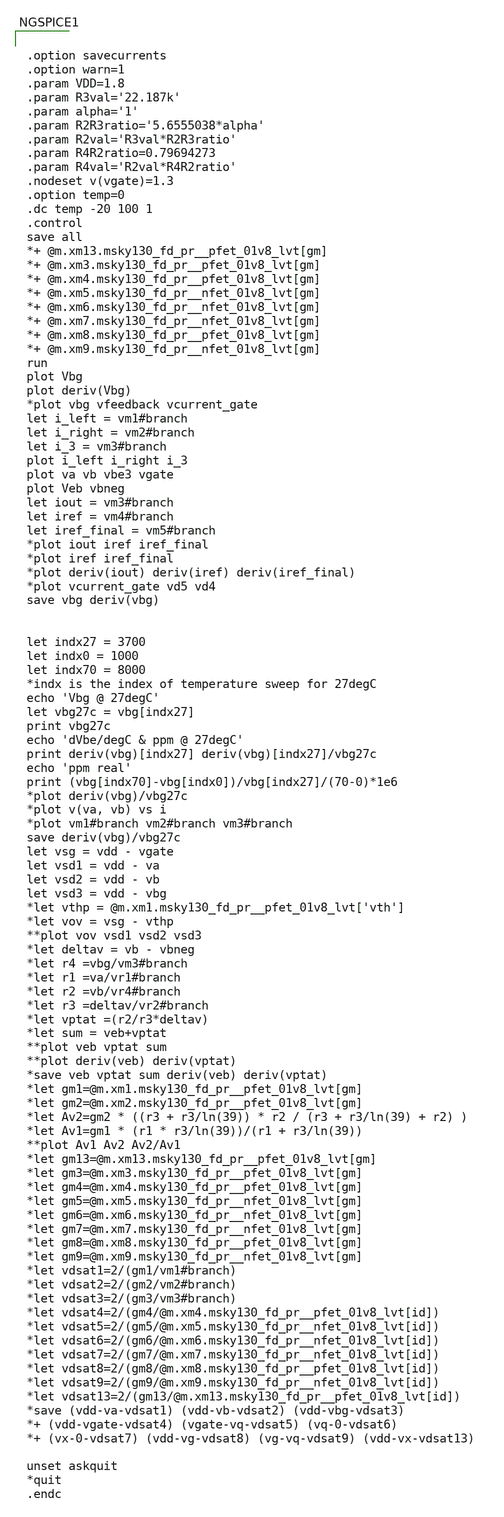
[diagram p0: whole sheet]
** sch_path: scratch.sch
**.subckt scratch
**** begin user architecture code


.options savecurrents


.option
.control
save all
let startR = 20k
let endR = 30k
let incre = 1k
let curR = startR
while curR le endR
alter Rt curR
dc temp -40 100 1
write dc.out Vbg
set appendwrite
let curR = curR + incre
end
run

plot dc1.Vbg dc2.Vbg dc3.Vbg dc4.Vbg dc5.Vbg dc6.Vbg dc7.Vbg dc8.Vbg dc9.Vbg dc10.Vbg


.endc

*** plot voltage coefficient
*Vdd VDD GND 3.3
*V_en en GND 3.3
*.dc Vdd 2 4 0.1
*.control
*run
*plot deriv(V(Vbgp))
*.endc

*** plot temperature coefficient
*Vdd VDD GND 3.3
*V_en en GND 3.3
*.dc temp -40 140 1
*.control
*run
*plot deriv(V(Vbgp))/1.202344
*.endc



*** enable pin
*Vdd VDD GND 3.3
*V_en en GND PULSE(0 3.3 0 200us 200us 600us 2000us 0)
*.tran 1u 2000us
*.control
*run
*plot V(en)
*plot -I(VDD)
*.endc




.option savecurrents
.option warn=1
.param VDD=1.8
.param R3val='22.187k'
.param alpha='1'
.param R2R3ratio='5.6555038*alpha'
.param R2val='R3val*R2R3ratio'
.param R4R2ratio=0.79694273
.param R4val='R2val*R4R2ratio'
.nodeset v(vgate)=1.3
.option temp=0
.dc temp -20 100 1
.control
save all
*+ @m.xm13.msky130_fd_pr__pfet_01v8_lvt[gm]
*+ @m.xm3.msky130_fd_pr__pfet_01v8_lvt[gm]
*+ @m.xm4.msky130_fd_pr__pfet_01v8_lvt[gm]
*+ @m.xm5.msky130_fd_pr__nfet_01v8_lvt[gm]
*+ @m.xm6.msky130_fd_pr__nfet_01v8_lvt[gm]
*+ @m.xm7.msky130_fd_pr__nfet_01v8_lvt[gm]
*+ @m.xm8.msky130_fd_pr__pfet_01v8_lvt[gm]
*+ @m.xm9.msky130_fd_pr__nfet_01v8_lvt[gm]
run
plot Vbg
plot deriv(Vbg)
*plot vbg vfeedback vcurrent_gate
let i_left = vm1#branch
let i_right = vm2#branch
let i_3 = vm3#branch
plot i_left i_right i_3
plot va vb vbe3 vgate
plot Veb vbneg
let iout = vm3#branch
let iref = vm4#branch
let iref_final = vm5#branch
*plot iout iref iref_final
*plot iref iref_final
*plot deriv(iout) deriv(iref) deriv(iref_final)
*plot vcurrent_gate vd5 vd4
save vbg deriv(vbg)


let indx27 = 3700
let indx0 = 1000
let indx70 = 8000
*indx is the index of temperature sweep for 27degC
echo 'Vbg @ 27degC'
let vbg27c = vbg[indx27]
print vbg27c
echo 'dVbe/degC & ppm @ 27degC'
print deriv(vbg)[indx27] deriv(vbg)[indx27]/vbg27c
echo 'ppm real'
print (vbg[indx70]-vbg[indx0])/vbg[indx27]/(70-0)*1e6
*plot deriv(vbg)/vbg27c
*plot v(va, vb) vs i
*plot vm1#branch vm2#branch vm3#branch
save deriv(vbg)/vbg27c
let vsg = vdd - vgate
let vsd1 = vdd - va
let vsd2 = vdd - vb
let vsd3 = vdd - vbg
*let vthp = @m.xm1.msky130_fd_pr__pfet_01v8_lvt['vth']
*let vov = vsg - vthp
**plot vov vsd1 vsd2 vsd3
*let deltav = vb - vbneg
*let r4 =vbg/vm3#branch
*let r1 =va/vr1#branch
*let r2 =vb/vr4#branch
*let r3 =deltav/vr2#branch
*let vptat =(r2/r3*deltav)
*let sum = veb+vptat
**plot veb vptat sum
**plot deriv(veb) deriv(vptat)
*save veb vptat sum deriv(veb) deriv(vptat)
*let gm1=@m.xm1.msky130_fd_pr__pfet_01v8_lvt[gm]
*let gm2=@m.xm2.msky130_fd_pr__pfet_01v8_lvt[gm]
*let Av2=gm2 * ((r3 + r3/ln(39)) * r2 / (r3 + r3/ln(39) + r2) )
*let Av1=gm1 * (r1 * r3/ln(39))/(r1 + r3/ln(39))
**plot Av1 Av2 Av2/Av1
*let gm13=@m.xm13.msky130_fd_pr__pfet_01v8_lvt[gm]
*let gm3=@m.xm3.msky130_fd_pr__pfet_01v8_lvt[gm]
*let gm4=@m.xm4.msky130_fd_pr__pfet_01v8_lvt[gm]
*let gm5=@m.xm5.msky130_fd_pr__nfet_01v8_lvt[gm]
*let gm6=@m.xm6.msky130_fd_pr__nfet_01v8_lvt[gm]
*let gm7=@m.xm7.msky130_fd_pr__nfet_01v8_lvt[gm]
*let gm8=@m.xm8.msky130_fd_pr__pfet_01v8_lvt[gm]
*let gm9=@m.xm9.msky130_fd_pr__nfet_01v8_lvt[gm]
*let vdsat1=2/(gm1/vm1#branch)
*let vdsat2=2/(gm2/vm2#branch)
*let vdsat3=2/(gm3/vm3#branch)
*let vdsat4=2/(gm4/@m.xm4.msky130_fd_pr__pfet_01v8_lvt[id])
*let vdsat5=2/(gm5/@m.xm5.msky130_fd_pr__nfet_01v8_lvt[id])
*let vdsat6=2/(gm6/@m.xm6.msky130_fd_pr__nfet_01v8_lvt[id])
*let vdsat7=2/(gm7/@m.xm7.msky130_fd_pr__nfet_01v8_lvt[id])
*let vdsat8=2/(gm8/@m.xm8.msky130_fd_pr__pfet_01v8_lvt[id])
*let vdsat9=2/(gm9/@m.xm9.msky130_fd_pr__nfet_01v8_lvt[id])
*let vdsat13=2/(gm13/@m.xm13.msky130_fd_pr__pfet_01v8_lvt[id])
*save (vdd-va-vdsat1) (vdd-vb-vdsat2) (vdd-vbg-vdsat3)
*+ (vdd-vgate-vdsat4) (vgate-vq-vdsat5) (vq-0-vdsat6)
*+ (vx-0-vdsat7) (vdd-vg-vdsat8) (vg-vq-vdsat9) (vdd-vx-vdsat13)

unset askquit
*quit
.endc


**** end user architecture code
**.ends
.end
